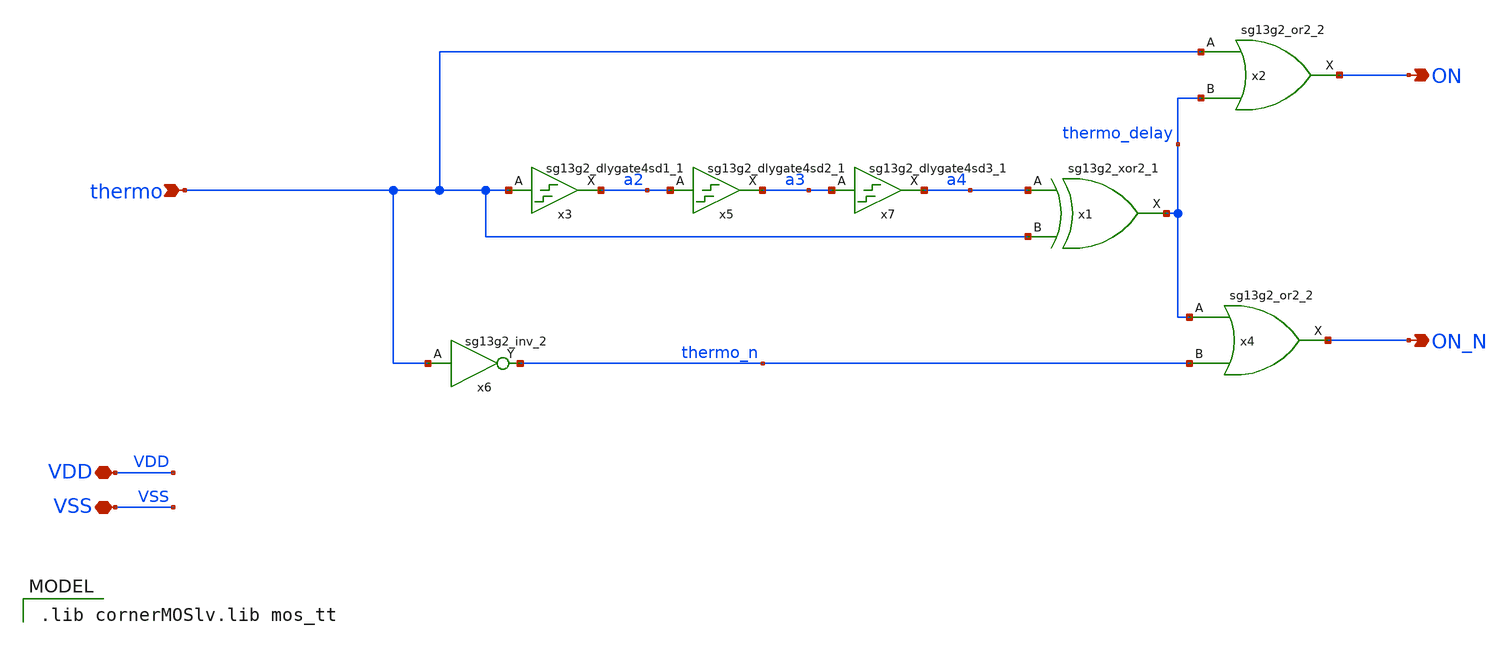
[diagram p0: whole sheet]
** sch_path: xschem/non_overlap.sch
* IHP-GmbH/IHP-Open-PDK/ihp-sg13g2/libs.tech/xschem/sg13g2_stdcells/sg13g2_dlygate4sd2_1.sch:
* Copyright 2023 IHP PDK Authors
* Licensed under the Apache License, Version 2.0 (the "License");
**.subckt non_overlap VSS thermo ON ON_N VDD
*.iopin VSS
*.ipin thermo
*.opin ON
*.opin ON_N
*.iopin VDD
x3 a2 thermo VDD VSS sg13g2_dlygate4sd1_1
x5 a3 a2 VDD VSS sg13g2_dlygate4sd2_1
x7 a4 a3 VDD VSS sg13g2_dlygate4sd3_1
x1 thermo_delay a4 thermo VDD VSS sg13g2_xor2_1
x2 ON thermo thermo_delay VDD VSS sg13g2_or2_2
x4 ON_N thermo_delay thermo_n VDD VSS sg13g2_or2_2
x6 thermo_n thermo VDD VSS sg13g2_inv_2
**** begin user architecture code
 .lib cornerMOSlv.lib mos_tt

**** end user architecture code
**.ends

* expanding   symbol:  sg13g2_stdcells/sg13g2_dlygate4sd1_1.sym # of pins=2
** sym_path: sg13g2_stdcells/sg13g2_dlygate4sd1_1.sym
** sch_path: sg13g2_stdcells/sg13g2_dlygate4sd1_1.sch
.subckt sg13g2_dlygate4sd1_1 X A VDD VSS
*.ipin A
*.opin X
*.iopin VDD
*.iopin VSS
XM1 net2 A VSS VSS sg13_lv_nmos w=420.00n l=130.00n ng=1 m=1 mm_ok=1
XM2 net1 net2 VSS VSS sg13_lv_nmos w=420.00n l=130.00n ng=1 m=1 mm_ok=1
XM3 net3 net1 VSS VSS sg13_lv_nmos w=420.00n l=130.00n ng=1 m=1 mm_ok=1
XM4 X net3 VSS VSS sg13_lv_nmos w=740.00n l=130.00n ng=1 m=1 mm_ok=1
XM5 net2 A VDD VDD sg13_lv_pmos w=420.00n l=130.00n ng=1 m=1 mm_ok=1
XM6 net1 net2 VDD VDD sg13_lv_pmos w=1.000u l=130.00n ng=1 m=1 mm_ok=1
XM7 net3 net1 VDD VDD sg13_lv_pmos w=1.000u l=130.00n ng=1 m=1 mm_ok=1
XM8 X net3 VDD VDD sg13_lv_pmos w=1.12u l=130.00n ng=1 m=1 mm_ok=1
.ends


* expanding   symbol:  sg13g2_stdcells/sg13g2_dlygate4sd2_1.sym # of pins=2
** sym_path: sg13g2_stdcells/sg13g2_dlygate4sd2_1.sym
** sch_path: sg13g2_stdcells/sg13g2_dlygate4sd2_1.sch
.subckt sg13g2_dlygate4sd2_1 X A VDD VSS
*.ipin A
*.opin X
*.iopin VDD
*.iopin VSS
XM1 net2 A VSS VSS sg13_lv_nmos w=420.00n l=130.00n ng=1 m=1 mm_ok=1
XM2 net1 net2 VSS VSS sg13_lv_nmos w=420.00n l=180.00n ng=1 m=1 mm_ok=1
XM3 net3 net1 VSS VSS sg13_lv_nmos w=420.00n l=180.00n ng=1 m=1 mm_ok=1
XM4 X net3 VSS VSS sg13_lv_nmos w=740.00n l=130.00n ng=1 m=1 mm_ok=1
XM5 net2 A VDD VDD sg13_lv_pmos w=420.00n l=130.00n ng=1 m=1 mm_ok=1
XM6 net1 net2 VDD VDD sg13_lv_pmos w=1.000u l=250.00n ng=1 m=1 mm_ok=1
XM7 net3 net1 VDD VDD sg13_lv_pmos w=1.000u l=250.00n ng=1 m=1 mm_ok=1
XM8 X net3 VDD VDD sg13_lv_pmos w=1.12u l=130.00n ng=1 m=1 mm_ok=1
.ends


* expanding   symbol:  sg13g2_stdcells/sg13g2_dlygate4sd3_1.sym # of pins=2
** sym_path: sg13g2_stdcells/sg13g2_dlygate4sd3_1.sym
** sch_path: sg13g2_stdcells/sg13g2_dlygate4sd3_1.sch
.subckt sg13g2_dlygate4sd3_1 X A VDD VSS
*.ipin A
*.opin X
*.iopin VDD
*.iopin VSS
XM1 net3 A VSS VSS sg13_lv_nmos w=420.00n l=130.00n ng=1 m=1 mm_ok=1
XM2 net1 net3 VSS VSS sg13_lv_nmos w=420.00n l=500.0n ng=1 m=1 mm_ok=1
XM3 net2 net1 VSS VSS sg13_lv_nmos w=420.00n l=500.0n ng=1 m=1 mm_ok=1
XM4 X net2 VSS VSS sg13_lv_nmos w=740.00n l=130.00n ng=1 m=1 mm_ok=1
XM5 net3 A VDD VDD sg13_lv_pmos w=420.00n l=130.00n ng=1 m=1 mm_ok=1
XM6 net1 net3 VDD VDD sg13_lv_pmos w=1.000u l=500.0n ng=1 m=1 mm_ok=1
XM7 net2 net1 VDD VDD sg13_lv_pmos w=1.000u l=500.0n ng=1 m=1 mm_ok=1
XM8 X net2 VDD VDD sg13_lv_pmos w=1.12u l=130.00n ng=1 m=1 mm_ok=1
.ends


* expanding   symbol:  sg13g2_stdcells/sg13g2_xor2_1.sym # of pins=3
** sym_path: sg13g2_stdcells/sg13g2_xor2_1.sym
** sch_path: sg13g2_stdcells/sg13g2_xor2_1.sch
.subckt sg13g2_xor2_1 X A B VDD VSS
*.opin X
*.ipin B
*.ipin A
*.iopin VDD
*.iopin VSS
XM1 net1 A VSS VSS sg13_lv_nmos w=550.00n l=130.00n ng=1 m=1 mm_ok=1
XM2 net1 B VSS VSS sg13_lv_nmos w=550.00n l=130.00n ng=1 m=1 mm_ok=1
XM3 X net1 VSS VSS sg13_lv_nmos w=740.00n l=130.00n ng=1 m=1 mm_ok=1
XM4 X B net3 VSS sg13_lv_nmos w=740.00n l=130.00n ng=1 m=1 mm_ok=1
XM5 net3 A VSS VSS sg13_lv_nmos w=740.00n l=130.00n ng=1 m=1 mm_ok=1
XM6 net4 A VDD VDD sg13_lv_pmos w=1.000u l=130.00n ng=1 m=1 mm_ok=1
XM7 net1 B net4 VDD sg13_lv_pmos w=1.000u l=130.00n ng=1 m=1 mm_ok=1
XM8 net2 A VDD VDD sg13_lv_pmos w=1.12u l=130.00n ng=1 m=1 mm_ok=1
XM9 X net1 net2 VDD sg13_lv_pmos w=1.12u l=130.00n ng=1 m=1 mm_ok=1
XM10 net2 B VDD VDD sg13_lv_pmos w=1.12u l=130.00n ng=1 m=1 mm_ok=1
.ends


* expanding   symbol:  sg13g2_stdcells/sg13g2_or2_2.sym # of pins=3
** sym_path: sg13g2_stdcells/sg13g2_or2_2.sym
** sch_path: sg13g2_stdcells/sg13g2_or2_2.sch
.subckt sg13g2_or2_2 X A B VDD VSS
*.opin X
*.ipin B
*.ipin A
*.iopin VDD
*.iopin VSS
XM1 net1 B VSS VSS sg13_lv_nmos w=550.00n l=130.00n ng=1 m=1 mm_ok=1
XM2 net1 A VSS VSS sg13_lv_nmos w=550.00n l=130.00n ng=1 m=1 mm_ok=1
XM3 X net1 VSS VSS sg13_lv_nmos w=1.48u l=130.00n ng=2 m=1 mm_ok=1
XM4 net2 A VDD VDD sg13_lv_pmos w=840.00n l=130.00n ng=1 m=1 mm_ok=1
XM5 net1 B net2 VDD sg13_lv_pmos w=840.00n l=130.00n ng=1 m=1 mm_ok=1
XM6 X net1 VDD VDD sg13_lv_pmos w=2.24u l=130.00n ng=2 m=1 mm_ok=1
.ends


* expanding   symbol:  sg13g2_stdcells/sg13g2_inv_2.sym # of pins=2
** sym_path: sg13g2_stdcells/sg13g2_inv_2.sym
** sch_path: sg13g2_stdcells/sg13g2_inv_2.sch
.subckt sg13g2_inv_2 Y A VDD VSS
*.opin Y
*.ipin A
*.iopin VDD
*.iopin VSS
XM1 Y A VSS VSS sg13_lv_nmos w=1.48u l=130.00n ng=2 m=1 mm_ok=1
XM2 Y A VDD VDD sg13_lv_pmos w=2.24u l=130.00n ng=2 m=1 mm_ok=1
.ends

.end
